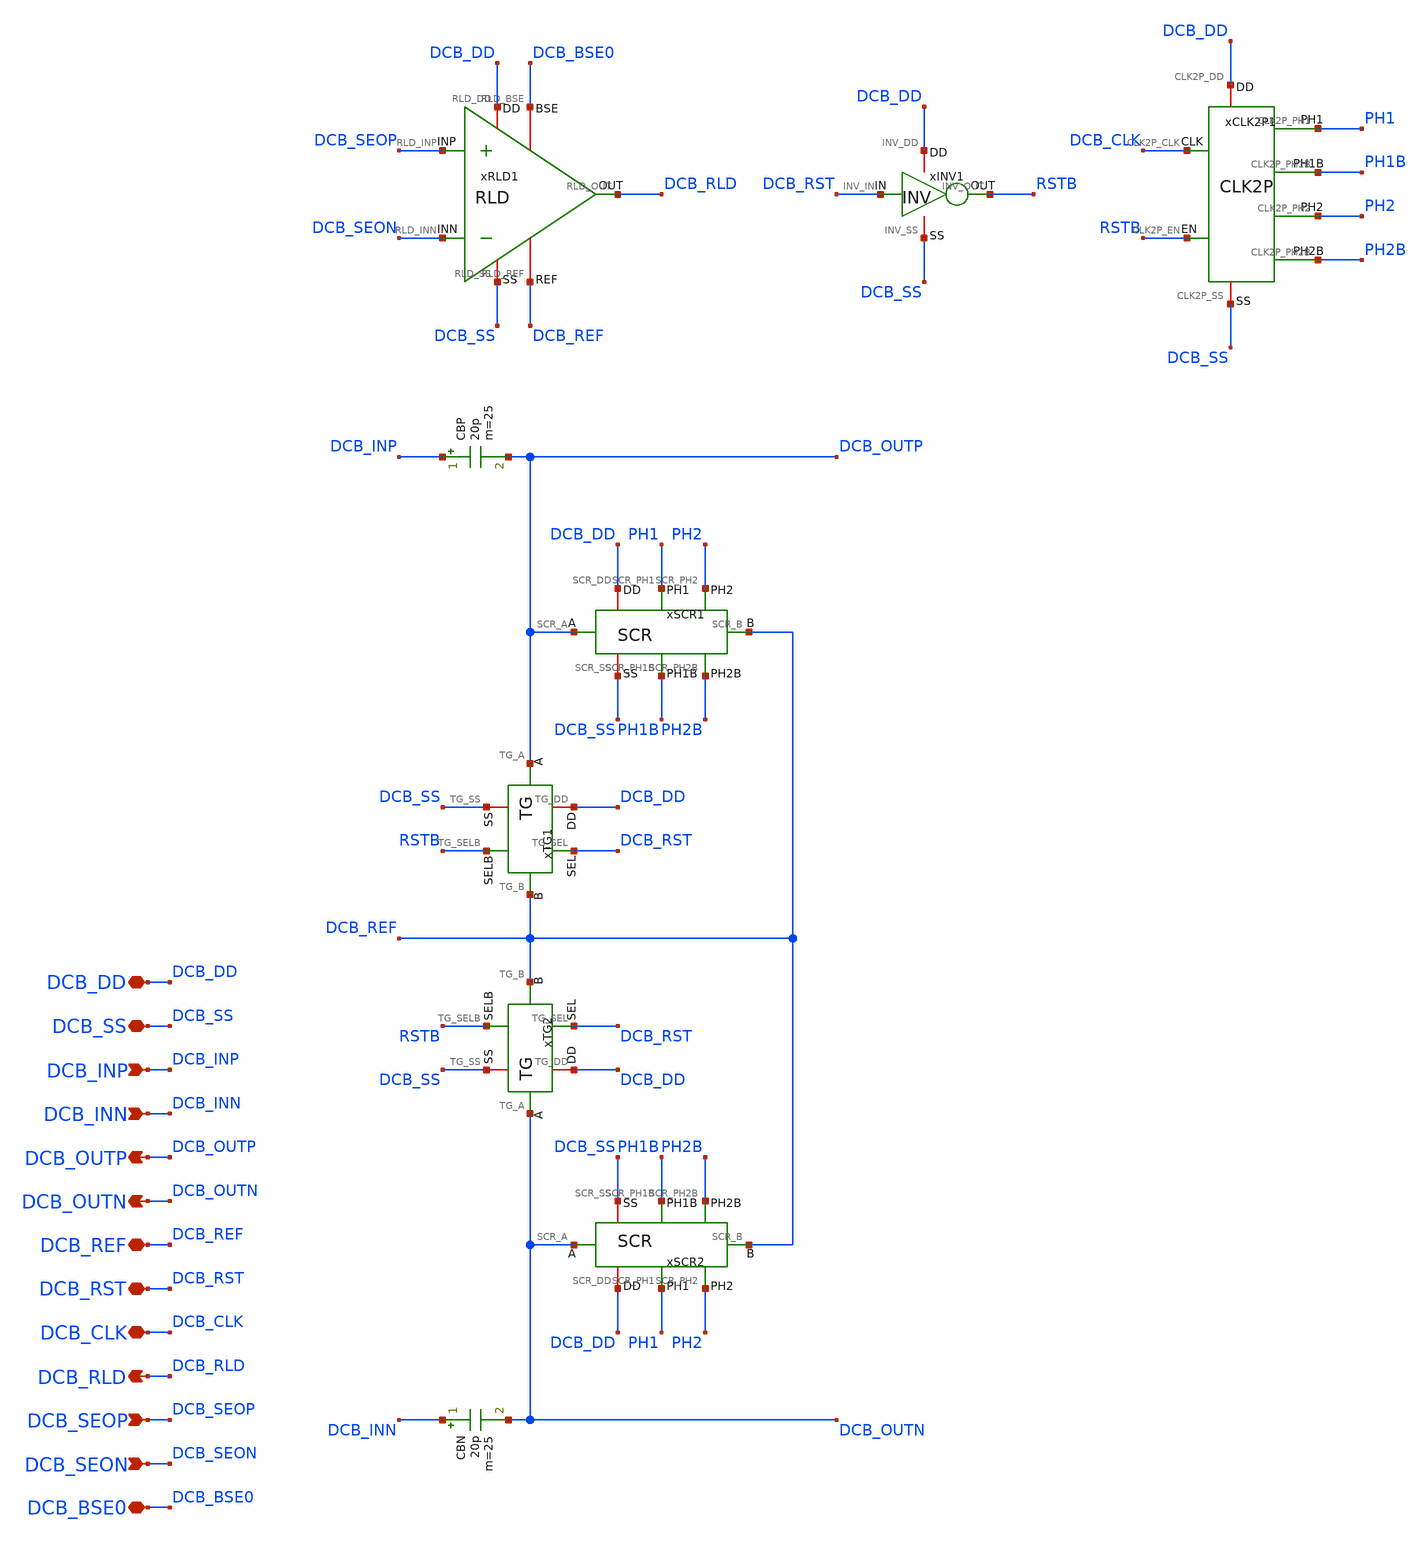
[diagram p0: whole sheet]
** sch_path: Design_Files/IC Design/Schematic/DCB/DCB.sch
**.subckt DCB DCB_DD DCB_SS DCB_INP DCB_INN DCB_OUTP DCB_OUTN DCB_REF DCB_RST DCB_CLK DCB_RLD
*+ DCB_SEOP DCB_SEON DCB_BSE0
*.iopin DCB_DD
*.iopin DCB_SS
*.ipin DCB_INP
*.ipin DCB_INN
*.opin DCB_OUTP
*.opin DCB_OUTN
*.iopin DCB_REF
*.iopin DCB_RST
*.iopin DCB_CLK
*.opin DCB_RLD
*.ipin DCB_SEOP
*.ipin DCB_SEON
*.iopin DCB_BSE0
xTG1 DCB_DD DCB_SS DCB_OUTP DCB_REF DCB_RST RSTB TG
xTG2 DCB_DD DCB_SS DCB_OUTN DCB_REF DCB_RST RSTB TG
xINV1 DCB_DD DCB_SS DCB_RST RSTB INV
xSCR1 DCB_DD DCB_SS DCB_OUTP PH1 PH1B PH2 PH2B DCB_REF SCR
xCLK2P1 DCB_DD DCB_SS DCB_CLK PH1 PH1B PH2 PH2B RSTB CLK2P
xRLD1 DCB_DD DCB_SS DCB_SEOP DCB_SEON DCB_RLD DCB_REF DCB_BSE0 RLD
xSCR2 DCB_DD DCB_SS DCB_OUTN PH1 PH1B PH2 PH2B DCB_REF SCR
CBP DCB_INP DCB_OUTP 20p m=25
CBN DCB_INN DCB_OUTN 20p m=25
**.ends
.end
